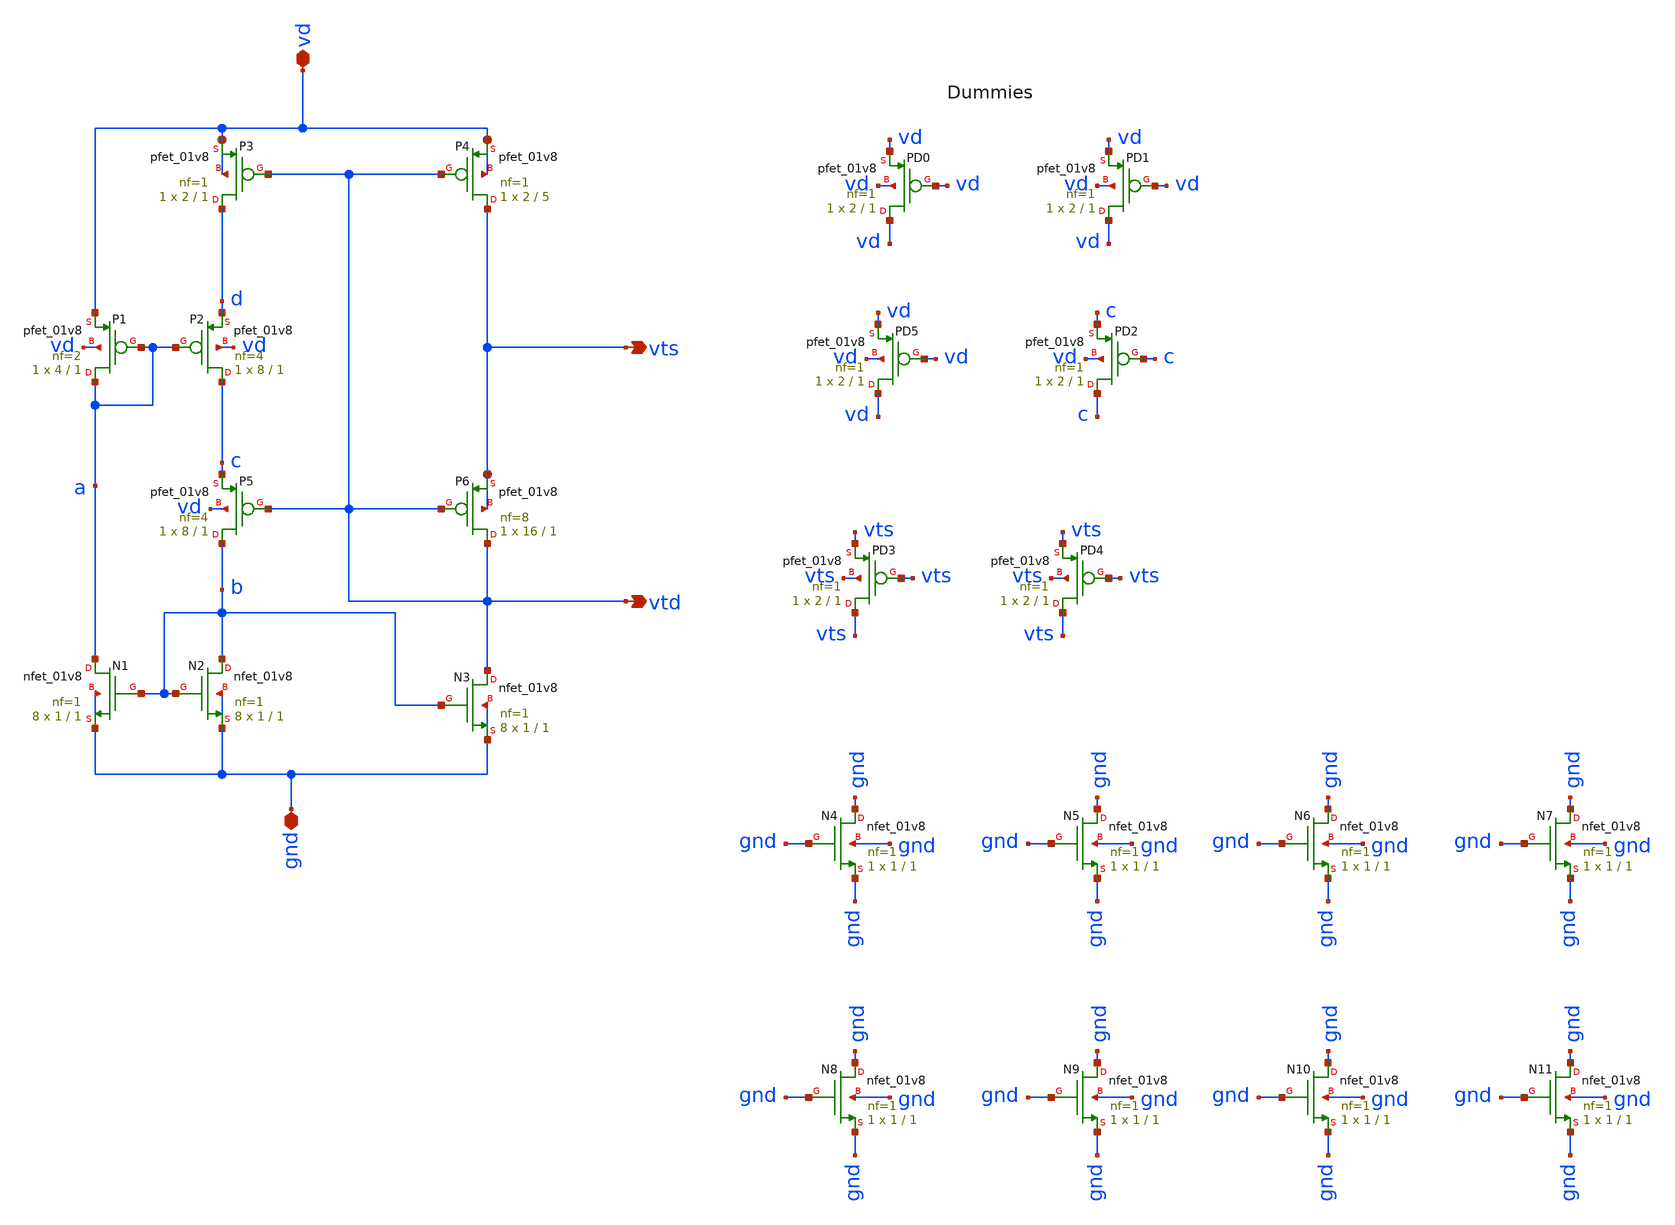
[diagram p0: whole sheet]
** sch_path: mag/sensor/xschem/sensor.sch
**.subckt sensor vd vts vtd gnd
*.iopin vd
*.opin vts
*.opin vtd
*.iopin gnd
XP1 a a vd vd sky130_fd_pr__pfet_01v8 L=1 W=4 nf=2 ad='int((nf+1)/2) * W/nf * 0.29' as='int((nf+2)/2) * W/nf * 0.29'
+ pd='2*int((nf+1)/2) * (W/nf + 0.29)' ps='2*int((nf+2)/2) * (W/nf + 0.29)' nrd='0.29 / W' nrs='0.29 / W'
+ sa=0 sb=0 sd=0 mult=1 m=1
XP2 c a d vd sky130_fd_pr__pfet_01v8 L=1 W=8 nf=4 ad='int((nf+1)/2) * W/nf * 0.29' as='int((nf+2)/2) * W/nf * 0.29'
+ pd='2*int((nf+1)/2) * (W/nf + 0.29)' ps='2*int((nf+2)/2) * (W/nf + 0.29)' nrd='0.29 / W' nrs='0.29 / W'
+ sa=0 sb=0 sd=0 mult=1 m=1
XP3 d vtd vd vd sky130_fd_pr__pfet_01v8 L=1 W=2 nf=1 ad='int((nf+1)/2) * W/nf * 0.29' as='int((nf+2)/2) * W/nf * 0.29'
+ pd='2*int((nf+1)/2) * (W/nf + 0.29)' ps='2*int((nf+2)/2) * (W/nf + 0.29)' nrd='0.29 / W' nrs='0.29 / W'
+ sa=0 sb=0 sd=0 mult=1 m=1
XP4 vts vtd vd vd sky130_fd_pr__pfet_01v8 L=5 W=2 nf=1 ad='int((nf+1)/2) * W/nf * 0.29' as='int((nf+2)/2) * W/nf * 0.29'
+ pd='2*int((nf+1)/2) * (W/nf + 0.29)' ps='2*int((nf+2)/2) * (W/nf + 0.29)' nrd='0.29 / W' nrs='0.29 / W'
+ sa=0 sb=0 sd=0 mult=1 m=1
XP5 b vtd c vd sky130_fd_pr__pfet_01v8 L=1 W=8 nf=4 ad='int((nf+1)/2) * W/nf * 0.29' as='int((nf+2)/2) * W/nf * 0.29'
+ pd='2*int((nf+1)/2) * (W/nf + 0.29)' ps='2*int((nf+2)/2) * (W/nf + 0.29)' nrd='0.29 / W' nrs='0.29 / W'
+ sa=0 sb=0 sd=0 mult=1 m=1
XP6 vtd vtd vts vts sky130_fd_pr__pfet_01v8 L=1 W=16 nf=8 ad='int((nf+1)/2) * W/nf * 0.29' as='int((nf+2)/2) * W/nf * 0.29'
+ pd='2*int((nf+1)/2) * (W/nf + 0.29)' ps='2*int((nf+2)/2) * (W/nf + 0.29)' nrd='0.29 / W' nrs='0.29 / W'
+ sa=0 sb=0 sd=0 mult=1 m=1
XN1 a b gnd gnd sky130_fd_pr__nfet_01v8 L=1 W=1 nf=1 ad='int((nf+1)/2) * W/nf * 0.29' as='int((nf+2)/2) * W/nf * 0.29'
+ pd='2*int((nf+1)/2) * (W/nf + 0.29)' ps='2*int((nf+2)/2) * (W/nf + 0.29)' nrd='0.29 / W' nrs='0.29 / W'
+ sa=0 sb=0 sd=0 mult=8 m=8
XN2 b b gnd gnd sky130_fd_pr__nfet_01v8 L=1 W=1 nf=1 ad='int((nf+1)/2) * W/nf * 0.29' as='int((nf+2)/2) * W/nf * 0.29'
+ pd='2*int((nf+1)/2) * (W/nf + 0.29)' ps='2*int((nf+2)/2) * (W/nf + 0.29)' nrd='0.29 / W' nrs='0.29 / W'
+ sa=0 sb=0 sd=0 mult=8 m=8
XN3 vtd b gnd gnd sky130_fd_pr__nfet_01v8 L=1 W=1 nf=1 ad='int((nf+1)/2) * W/nf * 0.29' as='int((nf+2)/2) * W/nf * 0.29'
+ pd='2*int((nf+1)/2) * (W/nf + 0.29)' ps='2*int((nf+2)/2) * (W/nf + 0.29)' nrd='0.29 / W' nrs='0.29 / W'
+ sa=0 sb=0 sd=0 mult=8 m=8
XPD0 vd vd vd vd sky130_fd_pr__pfet_01v8 L=1 W=2 nf=1 ad='int((nf+1)/2) * W/nf * 0.29' as='int((nf+2)/2) * W/nf * 0.29'
+ pd='2*int((nf+1)/2) * (W/nf + 0.29)' ps='2*int((nf+2)/2) * (W/nf + 0.29)' nrd='0.29 / W' nrs='0.29 / W'
+ sa=0 sb=0 sd=0 mult=1 m=1
XPD1 vd vd vd vd sky130_fd_pr__pfet_01v8 L=1 W=2 nf=1 ad='int((nf+1)/2) * W/nf * 0.29' as='int((nf+2)/2) * W/nf * 0.29'
+ pd='2*int((nf+1)/2) * (W/nf + 0.29)' ps='2*int((nf+2)/2) * (W/nf + 0.29)' nrd='0.29 / W' nrs='0.29 / W'
+ sa=0 sb=0 sd=0 mult=1 m=1
XPD2 c c c vd sky130_fd_pr__pfet_01v8 L=1 W=2 nf=1 ad='int((nf+1)/2) * W/nf * 0.29' as='int((nf+2)/2) * W/nf * 0.29'
+ pd='2*int((nf+1)/2) * (W/nf + 0.29)' ps='2*int((nf+2)/2) * (W/nf + 0.29)' nrd='0.29 / W' nrs='0.29 / W'
+ sa=0 sb=0 sd=0 mult=1 m=1
XPD3 vts vts vts vts sky130_fd_pr__pfet_01v8 L=1 W=2 nf=1 ad='int((nf+1)/2) * W/nf * 0.29' as='int((nf+2)/2) * W/nf * 0.29'
+ pd='2*int((nf+1)/2) * (W/nf + 0.29)' ps='2*int((nf+2)/2) * (W/nf + 0.29)' nrd='0.29 / W' nrs='0.29 / W'
+ sa=0 sb=0 sd=0 mult=1 m=1
XPD4 vts vts vts vts sky130_fd_pr__pfet_01v8 L=1 W=2 nf=1 ad='int((nf+1)/2) * W/nf * 0.29' as='int((nf+2)/2) * W/nf * 0.29'
+ pd='2*int((nf+1)/2) * (W/nf + 0.29)' ps='2*int((nf+2)/2) * (W/nf + 0.29)' nrd='0.29 / W' nrs='0.29 / W'
+ sa=0 sb=0 sd=0 mult=1 m=1
XPD5 vd vd vd vd sky130_fd_pr__pfet_01v8 L=1 W=2 nf=1 ad='int((nf+1)/2) * W/nf * 0.29' as='int((nf+2)/2) * W/nf * 0.29'
+ pd='2*int((nf+1)/2) * (W/nf + 0.29)' ps='2*int((nf+2)/2) * (W/nf + 0.29)' nrd='0.29 / W' nrs='0.29 / W'
+ sa=0 sb=0 sd=0 mult=1 m=1
XN4 gnd gnd gnd gnd sky130_fd_pr__nfet_01v8 L=1 W=1 nf=1 ad='int((nf+1)/2) * W/nf * 0.29' as='int((nf+2)/2) * W/nf * 0.29'
+ pd='2*int((nf+1)/2) * (W/nf + 0.29)' ps='2*int((nf+2)/2) * (W/nf + 0.29)' nrd='0.29 / W' nrs='0.29 / W'
+ sa=0 sb=0 sd=0 mult=1 m=1
XN5 gnd gnd gnd gnd sky130_fd_pr__nfet_01v8 L=1 W=1 nf=1 ad='int((nf+1)/2) * W/nf * 0.29' as='int((nf+2)/2) * W/nf * 0.29'
+ pd='2*int((nf+1)/2) * (W/nf + 0.29)' ps='2*int((nf+2)/2) * (W/nf + 0.29)' nrd='0.29 / W' nrs='0.29 / W'
+ sa=0 sb=0 sd=0 mult=1 m=1
XN6 gnd gnd gnd gnd sky130_fd_pr__nfet_01v8 L=1 W=1 nf=1 ad='int((nf+1)/2) * W/nf * 0.29' as='int((nf+2)/2) * W/nf * 0.29'
+ pd='2*int((nf+1)/2) * (W/nf + 0.29)' ps='2*int((nf+2)/2) * (W/nf + 0.29)' nrd='0.29 / W' nrs='0.29 / W'
+ sa=0 sb=0 sd=0 mult=1 m=1
XN7 gnd gnd gnd gnd sky130_fd_pr__nfet_01v8 L=1 W=1 nf=1 ad='int((nf+1)/2) * W/nf * 0.29' as='int((nf+2)/2) * W/nf * 0.29'
+ pd='2*int((nf+1)/2) * (W/nf + 0.29)' ps='2*int((nf+2)/2) * (W/nf + 0.29)' nrd='0.29 / W' nrs='0.29 / W'
+ sa=0 sb=0 sd=0 mult=1 m=1
XN8 gnd gnd gnd gnd sky130_fd_pr__nfet_01v8 L=1 W=1 nf=1 ad='int((nf+1)/2) * W/nf * 0.29' as='int((nf+2)/2) * W/nf * 0.29'
+ pd='2*int((nf+1)/2) * (W/nf + 0.29)' ps='2*int((nf+2)/2) * (W/nf + 0.29)' nrd='0.29 / W' nrs='0.29 / W'
+ sa=0 sb=0 sd=0 mult=1 m=1
XN9 gnd gnd gnd gnd sky130_fd_pr__nfet_01v8 L=1 W=1 nf=1 ad='int((nf+1)/2) * W/nf * 0.29' as='int((nf+2)/2) * W/nf * 0.29'
+ pd='2*int((nf+1)/2) * (W/nf + 0.29)' ps='2*int((nf+2)/2) * (W/nf + 0.29)' nrd='0.29 / W' nrs='0.29 / W'
+ sa=0 sb=0 sd=0 mult=1 m=1
XN10 gnd gnd gnd gnd sky130_fd_pr__nfet_01v8 L=1 W=1 nf=1 ad='int((nf+1)/2) * W/nf * 0.29' as='int((nf+2)/2) * W/nf * 0.29'
+ pd='2*int((nf+1)/2) * (W/nf + 0.29)' ps='2*int((nf+2)/2) * (W/nf + 0.29)' nrd='0.29 / W' nrs='0.29 / W'
+ sa=0 sb=0 sd=0 mult=1 m=1
XN11 gnd gnd gnd gnd sky130_fd_pr__nfet_01v8 L=1 W=1 nf=1 ad='int((nf+1)/2) * W/nf * 0.29' as='int((nf+2)/2) * W/nf * 0.29'
+ pd='2*int((nf+1)/2) * (W/nf + 0.29)' ps='2*int((nf+2)/2) * (W/nf + 0.29)' nrd='0.29 / W' nrs='0.29 / W'
+ sa=0 sb=0 sd=0 mult=1 m=1
**.ends
.end
